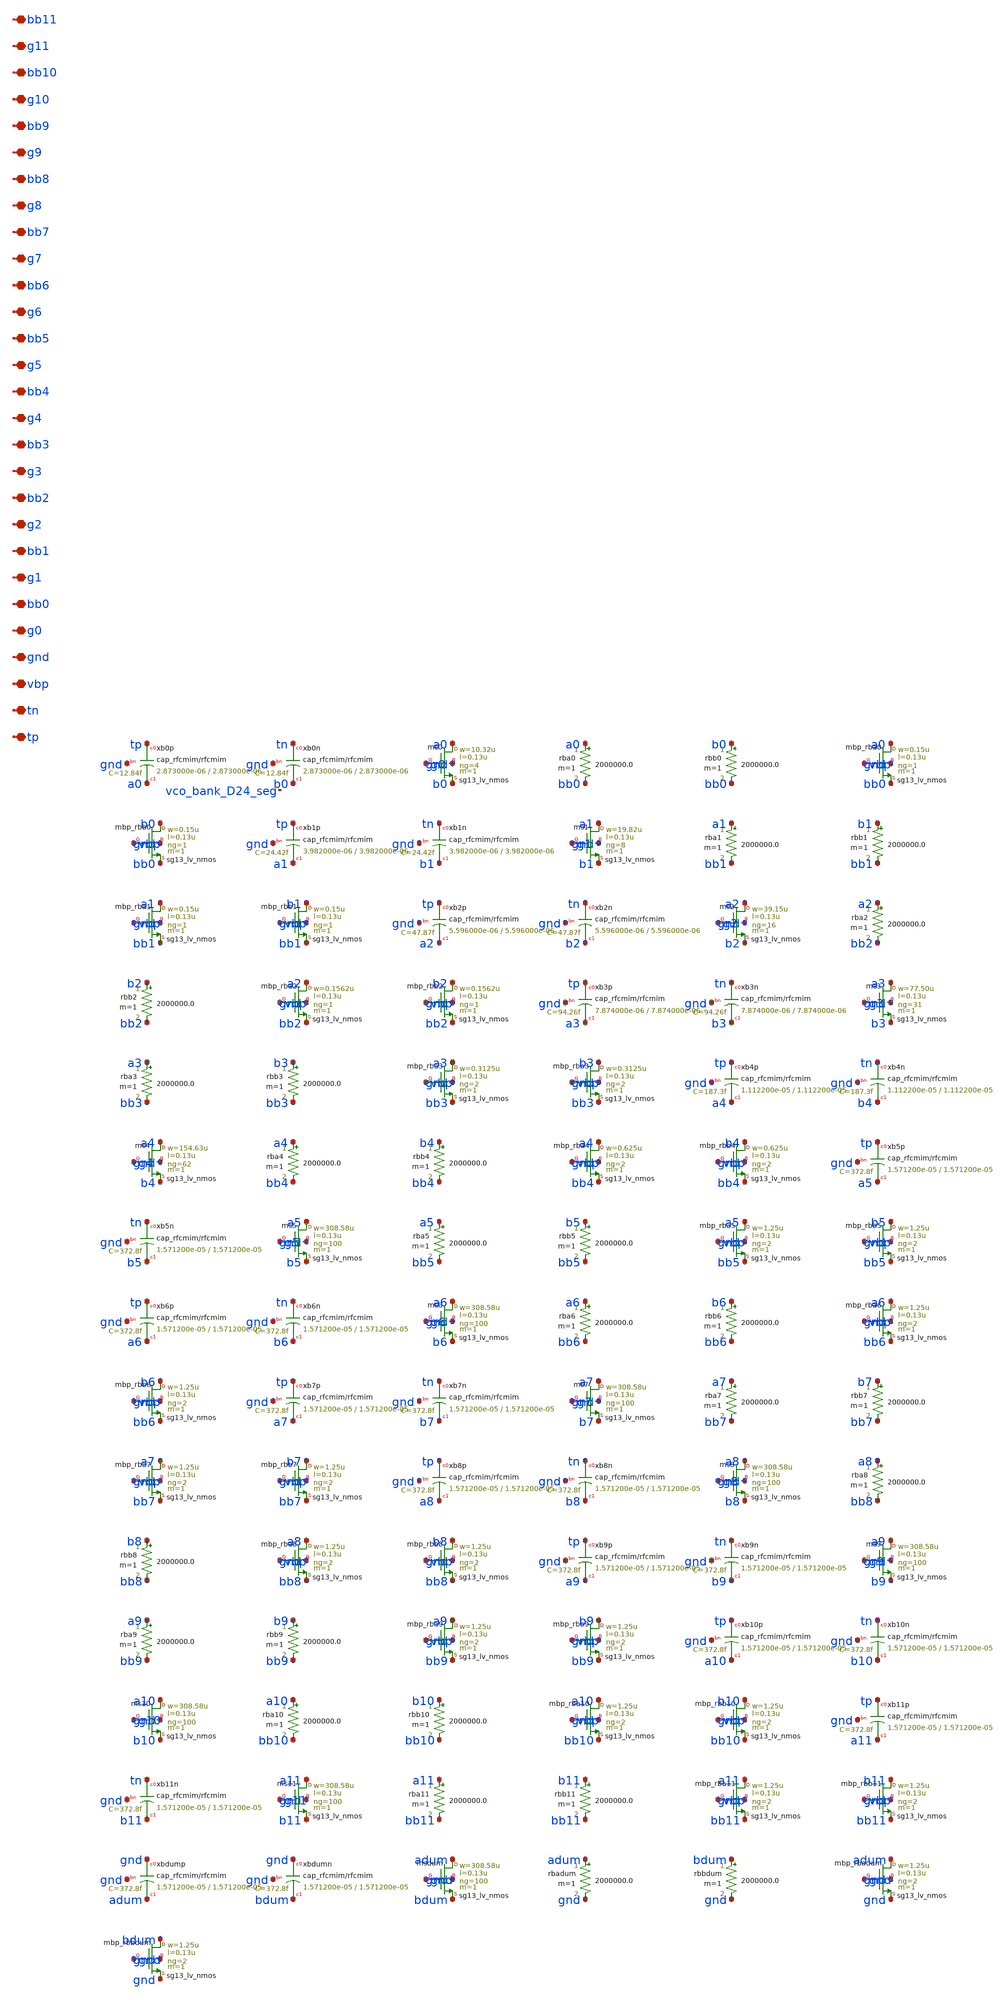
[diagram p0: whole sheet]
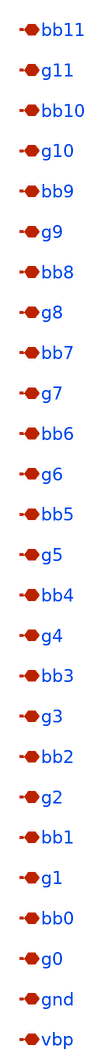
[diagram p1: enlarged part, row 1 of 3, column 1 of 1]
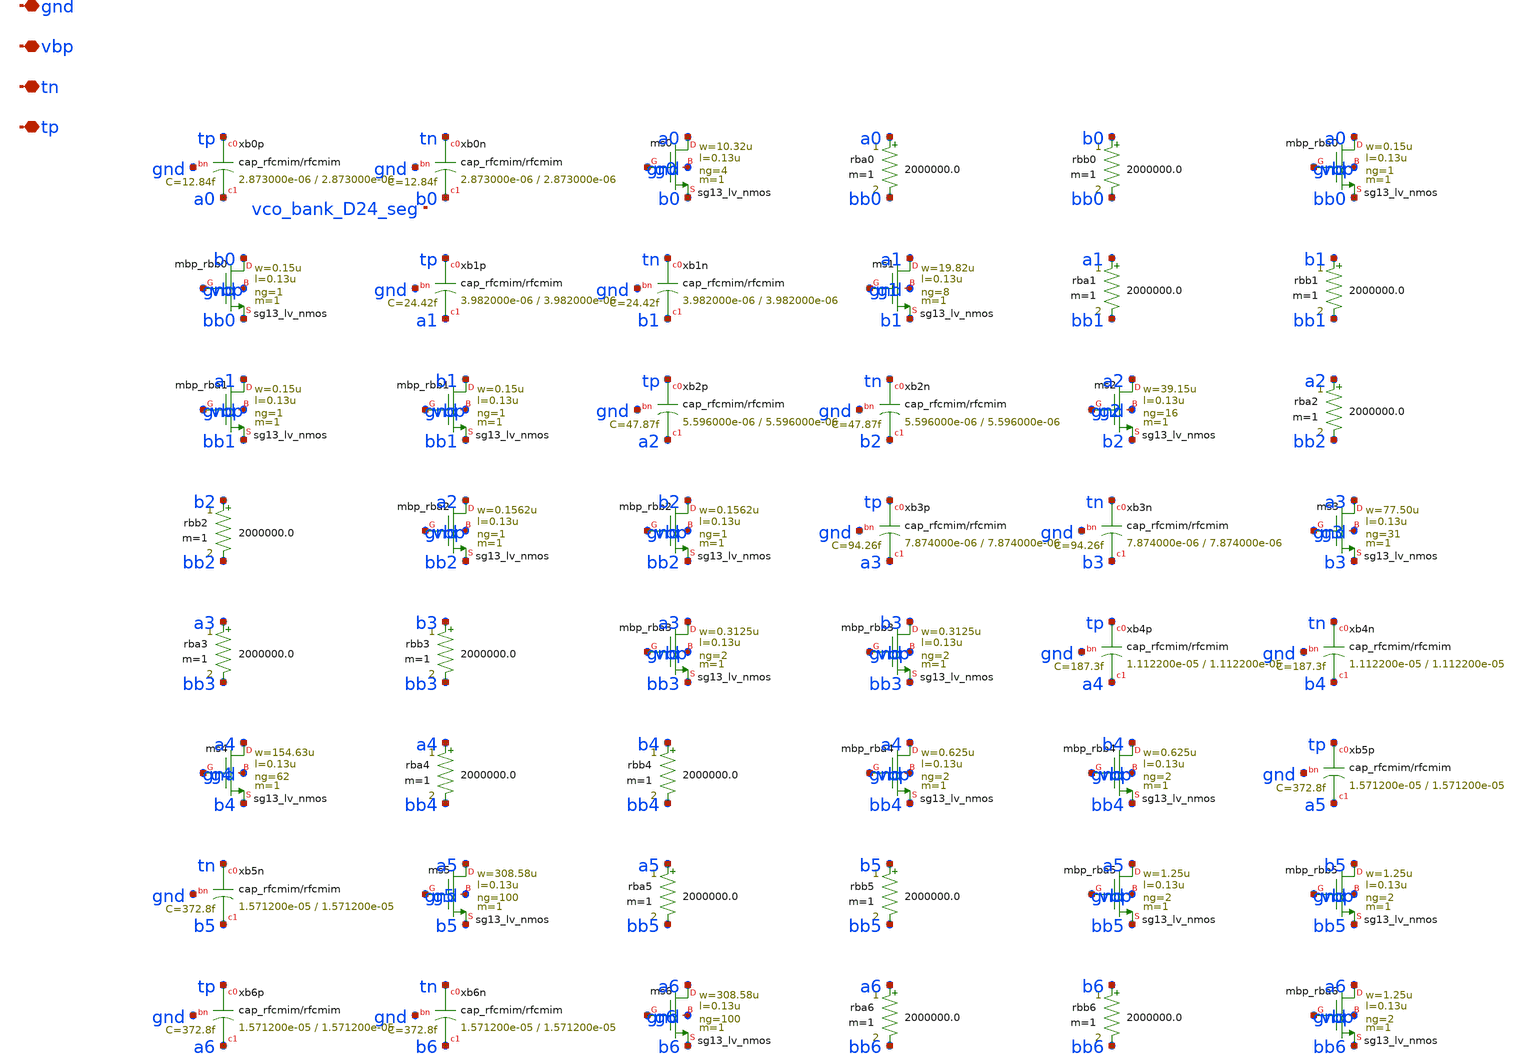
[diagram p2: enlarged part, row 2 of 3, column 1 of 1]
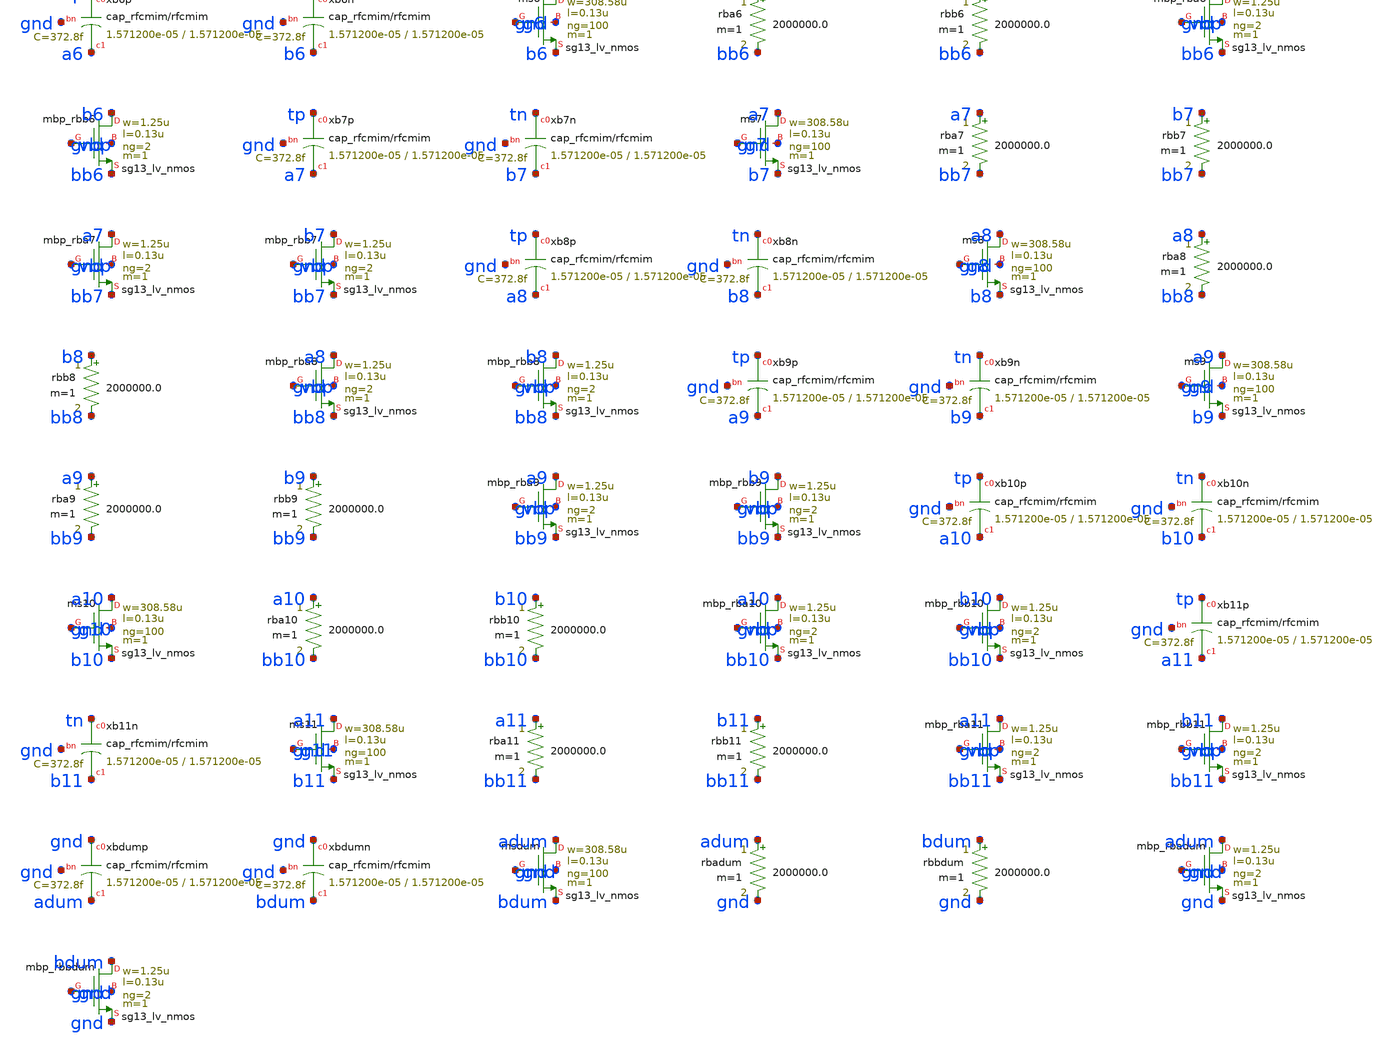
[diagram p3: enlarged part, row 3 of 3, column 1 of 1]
** sch_path: analog/vco/sch/vco_bank.sch
**.subckt vco_bank tp tn vbp gnd g0 bb0 g1 bb1 g2 bb2 g3 bb3 g4 bb4 g5 bb5 g6 bb6 g7 bb7 g8 bb8 g9
*+ bb9 g10 bb10 g11 bb11
*.iopin tp
*.iopin tn
*.iopin vbp
*.iopin gnd
*.iopin g0
*.iopin bb0
*.iopin g1
*.iopin bb1
*.iopin g2
*.iopin bb2
*.iopin g3
*.iopin bb3
*.iopin g4
*.iopin bb4
*.iopin g5
*.iopin bb5
*.iopin g6
*.iopin bb6
*.iopin g7
*.iopin bb7
*.iopin g8
*.iopin bb8
*.iopin g9
*.iopin bb9
*.iopin g10
*.iopin bb10
*.iopin g11
*.iopin bb11
Xxb0p tp a0 gnd cap_rfcmim w=2.873000e-06 l=2.873000e-06 wfeed=5.0e-6 m=1 mm_ok=1
Xxb0n tn b0 gnd cap_rfcmim w=2.873000e-06 l=2.873000e-06 wfeed=5.0e-6 m=1 mm_ok=1
Xms0 a0 g0 b0 gnd sg13_lv_nmos w=10.32u l=0.13u ng=4 m=1 mm_ok=1
rba0 a0 bb0 2000000.0 m=1
rbb0 b0 bb0 2000000.0 m=1
Xmbp_rba0 a0 vbp bb0 gnd sg13_lv_nmos w=0.15u l=0.13u ng=1 m=1 mm_ok=1
Xmbp_rbb0 b0 vbp bb0 gnd sg13_lv_nmos w=0.15u l=0.13u ng=1 m=1 mm_ok=1
Xxb1p tp a1 gnd cap_rfcmim w=3.982000e-06 l=3.982000e-06 wfeed=5.0e-6 m=1 mm_ok=1
Xxb1n tn b1 gnd cap_rfcmim w=3.982000e-06 l=3.982000e-06 wfeed=5.0e-6 m=1 mm_ok=1
Xms1 a1 g1 b1 gnd sg13_lv_nmos w=19.82u l=0.13u ng=8 m=1 mm_ok=1
rba1 a1 bb1 2000000.0 m=1
rbb1 b1 bb1 2000000.0 m=1
Xmbp_rba1 a1 vbp bb1 gnd sg13_lv_nmos w=0.15u l=0.13u ng=1 m=1 mm_ok=1
Xmbp_rbb1 b1 vbp bb1 gnd sg13_lv_nmos w=0.15u l=0.13u ng=1 m=1 mm_ok=1
Xxb2p tp a2 gnd cap_rfcmim w=5.596000e-06 l=5.596000e-06 wfeed=5.0e-6 m=1 mm_ok=1
Xxb2n tn b2 gnd cap_rfcmim w=5.596000e-06 l=5.596000e-06 wfeed=5.0e-6 m=1 mm_ok=1
Xms2 a2 g2 b2 gnd sg13_lv_nmos w=39.15u l=0.13u ng=16 m=1 mm_ok=1
rba2 a2 bb2 2000000.0 m=1
rbb2 b2 bb2 2000000.0 m=1
Xmbp_rba2 a2 vbp bb2 gnd sg13_lv_nmos w=0.1562u l=0.13u ng=1 m=1 mm_ok=1
Xmbp_rbb2 b2 vbp bb2 gnd sg13_lv_nmos w=0.1562u l=0.13u ng=1 m=1 mm_ok=1
Xxb3p tp a3 gnd cap_rfcmim w=7.874000e-06 l=7.874000e-06 wfeed=5.0e-6 m=1 mm_ok=1
Xxb3n tn b3 gnd cap_rfcmim w=7.874000e-06 l=7.874000e-06 wfeed=5.0e-6 m=1 mm_ok=1
Xms3 a3 g3 b3 gnd sg13_lv_nmos w=77.50u l=0.13u ng=31 m=1 mm_ok=1
rba3 a3 bb3 2000000.0 m=1
rbb3 b3 bb3 2000000.0 m=1
Xmbp_rba3 a3 vbp bb3 gnd sg13_lv_nmos w=0.3125u l=0.13u ng=2 m=1 mm_ok=1
Xmbp_rbb3 b3 vbp bb3 gnd sg13_lv_nmos w=0.3125u l=0.13u ng=2 m=1 mm_ok=1
Xxb4p tp a4 gnd cap_rfcmim w=1.112200e-05 l=1.112200e-05 wfeed=5.0e-6 m=1 mm_ok=1
Xxb4n tn b4 gnd cap_rfcmim w=1.112200e-05 l=1.112200e-05 wfeed=5.0e-6 m=1 mm_ok=1
Xms4 a4 g4 b4 gnd sg13_lv_nmos w=154.63u l=0.13u ng=62 m=1 mm_ok=1
rba4 a4 bb4 2000000.0 m=1
rbb4 b4 bb4 2000000.0 m=1
Xmbp_rba4 a4 vbp bb4 gnd sg13_lv_nmos w=0.625u l=0.13u ng=2 m=1 mm_ok=1
Xmbp_rbb4 b4 vbp bb4 gnd sg13_lv_nmos w=0.625u l=0.13u ng=2 m=1 mm_ok=1
Xxb5p tp a5 gnd cap_rfcmim w=1.571200e-05 l=1.571200e-05 wfeed=5.0e-6 m=1 mm_ok=1
Xxb5n tn b5 gnd cap_rfcmim w=1.571200e-05 l=1.571200e-05 wfeed=5.0e-6 m=1 mm_ok=1
Xms5 a5 g5 b5 gnd sg13_lv_nmos w=308.58u l=0.13u ng=100 m=1 mm_ok=1
rba5 a5 bb5 2000000.0 m=1
rbb5 b5 bb5 2000000.0 m=1
Xmbp_rba5 a5 vbp bb5 gnd sg13_lv_nmos w=1.25u l=0.13u ng=2 m=1 mm_ok=1
Xmbp_rbb5 b5 vbp bb5 gnd sg13_lv_nmos w=1.25u l=0.13u ng=2 m=1 mm_ok=1
Xxb6p tp a6 gnd cap_rfcmim w=1.571200e-05 l=1.571200e-05 wfeed=5.0e-6 m=1 mm_ok=1
Xxb6n tn b6 gnd cap_rfcmim w=1.571200e-05 l=1.571200e-05 wfeed=5.0e-6 m=1 mm_ok=1
Xms6 a6 g6 b6 gnd sg13_lv_nmos w=308.58u l=0.13u ng=100 m=1 mm_ok=1
rba6 a6 bb6 2000000.0 m=1
rbb6 b6 bb6 2000000.0 m=1
Xmbp_rba6 a6 vbp bb6 gnd sg13_lv_nmos w=1.25u l=0.13u ng=2 m=1 mm_ok=1
Xmbp_rbb6 b6 vbp bb6 gnd sg13_lv_nmos w=1.25u l=0.13u ng=2 m=1 mm_ok=1
Xxb7p tp a7 gnd cap_rfcmim w=1.571200e-05 l=1.571200e-05 wfeed=5.0e-6 m=1 mm_ok=1
Xxb7n tn b7 gnd cap_rfcmim w=1.571200e-05 l=1.571200e-05 wfeed=5.0e-6 m=1 mm_ok=1
Xms7 a7 g7 b7 gnd sg13_lv_nmos w=308.58u l=0.13u ng=100 m=1 mm_ok=1
rba7 a7 bb7 2000000.0 m=1
rbb7 b7 bb7 2000000.0 m=1
Xmbp_rba7 a7 vbp bb7 gnd sg13_lv_nmos w=1.25u l=0.13u ng=2 m=1 mm_ok=1
Xmbp_rbb7 b7 vbp bb7 gnd sg13_lv_nmos w=1.25u l=0.13u ng=2 m=1 mm_ok=1
Xxb8p tp a8 gnd cap_rfcmim w=1.571200e-05 l=1.571200e-05 wfeed=5.0e-6 m=1 mm_ok=1
Xxb8n tn b8 gnd cap_rfcmim w=1.571200e-05 l=1.571200e-05 wfeed=5.0e-6 m=1 mm_ok=1
Xms8 a8 g8 b8 gnd sg13_lv_nmos w=308.58u l=0.13u ng=100 m=1 mm_ok=1
rba8 a8 bb8 2000000.0 m=1
rbb8 b8 bb8 2000000.0 m=1
Xmbp_rba8 a8 vbp bb8 gnd sg13_lv_nmos w=1.25u l=0.13u ng=2 m=1 mm_ok=1
Xmbp_rbb8 b8 vbp bb8 gnd sg13_lv_nmos w=1.25u l=0.13u ng=2 m=1 mm_ok=1
Xxb9p tp a9 gnd cap_rfcmim w=1.571200e-05 l=1.571200e-05 wfeed=5.0e-6 m=1 mm_ok=1
Xxb9n tn b9 gnd cap_rfcmim w=1.571200e-05 l=1.571200e-05 wfeed=5.0e-6 m=1 mm_ok=1
Xms9 a9 g9 b9 gnd sg13_lv_nmos w=308.58u l=0.13u ng=100 m=1 mm_ok=1
rba9 a9 bb9 2000000.0 m=1
rbb9 b9 bb9 2000000.0 m=1
Xmbp_rba9 a9 vbp bb9 gnd sg13_lv_nmos w=1.25u l=0.13u ng=2 m=1 mm_ok=1
Xmbp_rbb9 b9 vbp bb9 gnd sg13_lv_nmos w=1.25u l=0.13u ng=2 m=1 mm_ok=1
Xxb10p tp a10 gnd cap_rfcmim w=1.571200e-05 l=1.571200e-05 wfeed=5.0e-6 m=1 mm_ok=1
Xxb10n tn b10 gnd cap_rfcmim w=1.571200e-05 l=1.571200e-05 wfeed=5.0e-6 m=1 mm_ok=1
Xms10 a10 g10 b10 gnd sg13_lv_nmos w=308.58u l=0.13u ng=100 m=1 mm_ok=1
rba10 a10 bb10 2000000.0 m=1
rbb10 b10 bb10 2000000.0 m=1
Xmbp_rba10 a10 vbp bb10 gnd sg13_lv_nmos w=1.25u l=0.13u ng=2 m=1 mm_ok=1
Xmbp_rbb10 b10 vbp bb10 gnd sg13_lv_nmos w=1.25u l=0.13u ng=2 m=1 mm_ok=1
Xxb11p tp a11 gnd cap_rfcmim w=1.571200e-05 l=1.571200e-05 wfeed=5.0e-6 m=1 mm_ok=1
Xxb11n tn b11 gnd cap_rfcmim w=1.571200e-05 l=1.571200e-05 wfeed=5.0e-6 m=1 mm_ok=1
Xms11 a11 g11 b11 gnd sg13_lv_nmos w=308.58u l=0.13u ng=100 m=1 mm_ok=1
rba11 a11 bb11 2000000.0 m=1
rbb11 b11 bb11 2000000.0 m=1
Xmbp_rba11 a11 vbp bb11 gnd sg13_lv_nmos w=1.25u l=0.13u ng=2 m=1 mm_ok=1
Xmbp_rbb11 b11 vbp bb11 gnd sg13_lv_nmos w=1.25u l=0.13u ng=2 m=1 mm_ok=1
Xxbdump gnd adum gnd cap_rfcmim w=1.571200e-05 l=1.571200e-05 wfeed=5.0e-6 m=1 mm_ok=1
Xxbdumn gnd bdum gnd cap_rfcmim w=1.571200e-05 l=1.571200e-05 wfeed=5.0e-6 m=1 mm_ok=1
Xmsdum adum gnd bdum gnd sg13_lv_nmos w=308.58u l=0.13u ng=100 m=1 mm_ok=1
rbadum adum gnd 2000000.0 m=1
rbbdum bdum gnd 2000000.0 m=1
Xmbp_rbadum adum gnd gnd gnd sg13_lv_nmos w=1.25u l=0.13u ng=2 m=1 mm_ok=1
Xmbp_rbbdum bdum gnd gnd gnd sg13_lv_nmos w=1.25u l=0.13u ng=2 m=1 mm_ok=1
**.ends
.end
